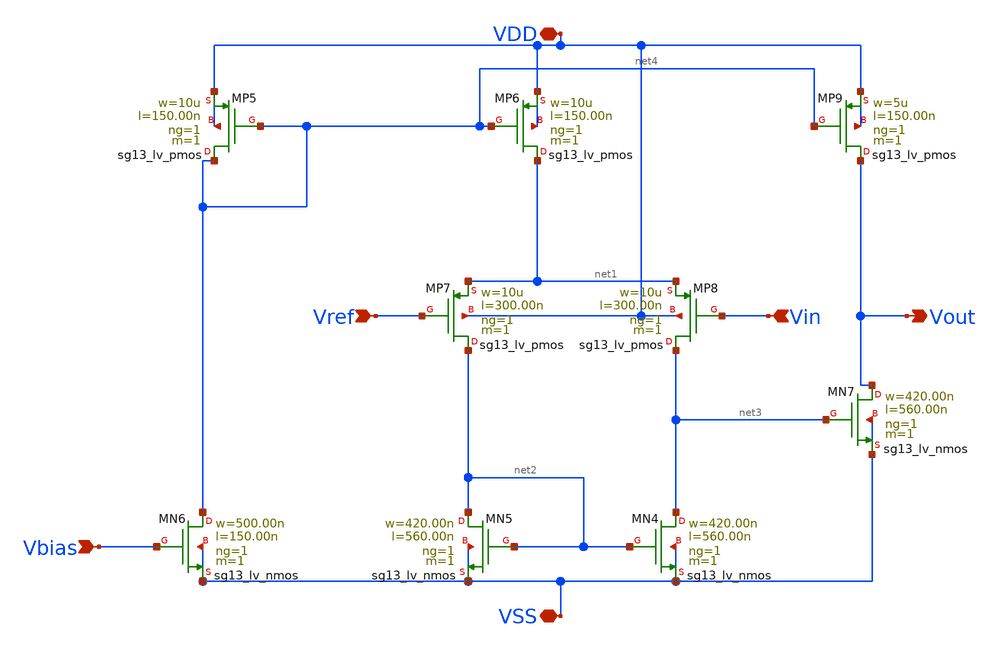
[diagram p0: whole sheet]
** sch_path: schematic/Opamp.sch
**.subckt Opamp Vin VDD VSS Vref Vout Vbias
*.ipin Vin
*.iopin VDD
*.iopin VSS
*.ipin Vref
*.opin Vout
*.ipin Vbias
XMP5 net4 net4 VDD VDD sg13_lv_pmos w=10u l=150.00n ng=1 m=1 mm_ok=1
XMP6 net1 net4 VDD VDD sg13_lv_pmos w=10u l=150.00n ng=1 m=1 mm_ok=1
XMN4 net3 net2 VSS VSS sg13_lv_nmos w=420.00n l=560.00n ng=1 m=1 mm_ok=1
XMN5 net2 net2 VSS VSS sg13_lv_nmos w=420.00n l=560.00n ng=1 m=1 mm_ok=1
XMN6 net4 Vbias VSS VSS sg13_lv_nmos w=500.00n l=150.00n ng=1 m=1 mm_ok=1
XMP7 net2 Vref net1 VDD sg13_lv_pmos w=10u l=300.00n ng=1 m=1 mm_ok=1
XMP8 net3 Vin net1 VDD sg13_lv_pmos w=10u l=300.00n ng=1 m=1 mm_ok=1
XMN7 Vout net3 VSS VSS sg13_lv_nmos w=420.00n l=560.00n ng=1 m=1 mm_ok=1
XMP9 Vout net4 VDD VDD sg13_lv_pmos w=5u l=150.00n ng=1 m=1 mm_ok=1
**.ends
.end
